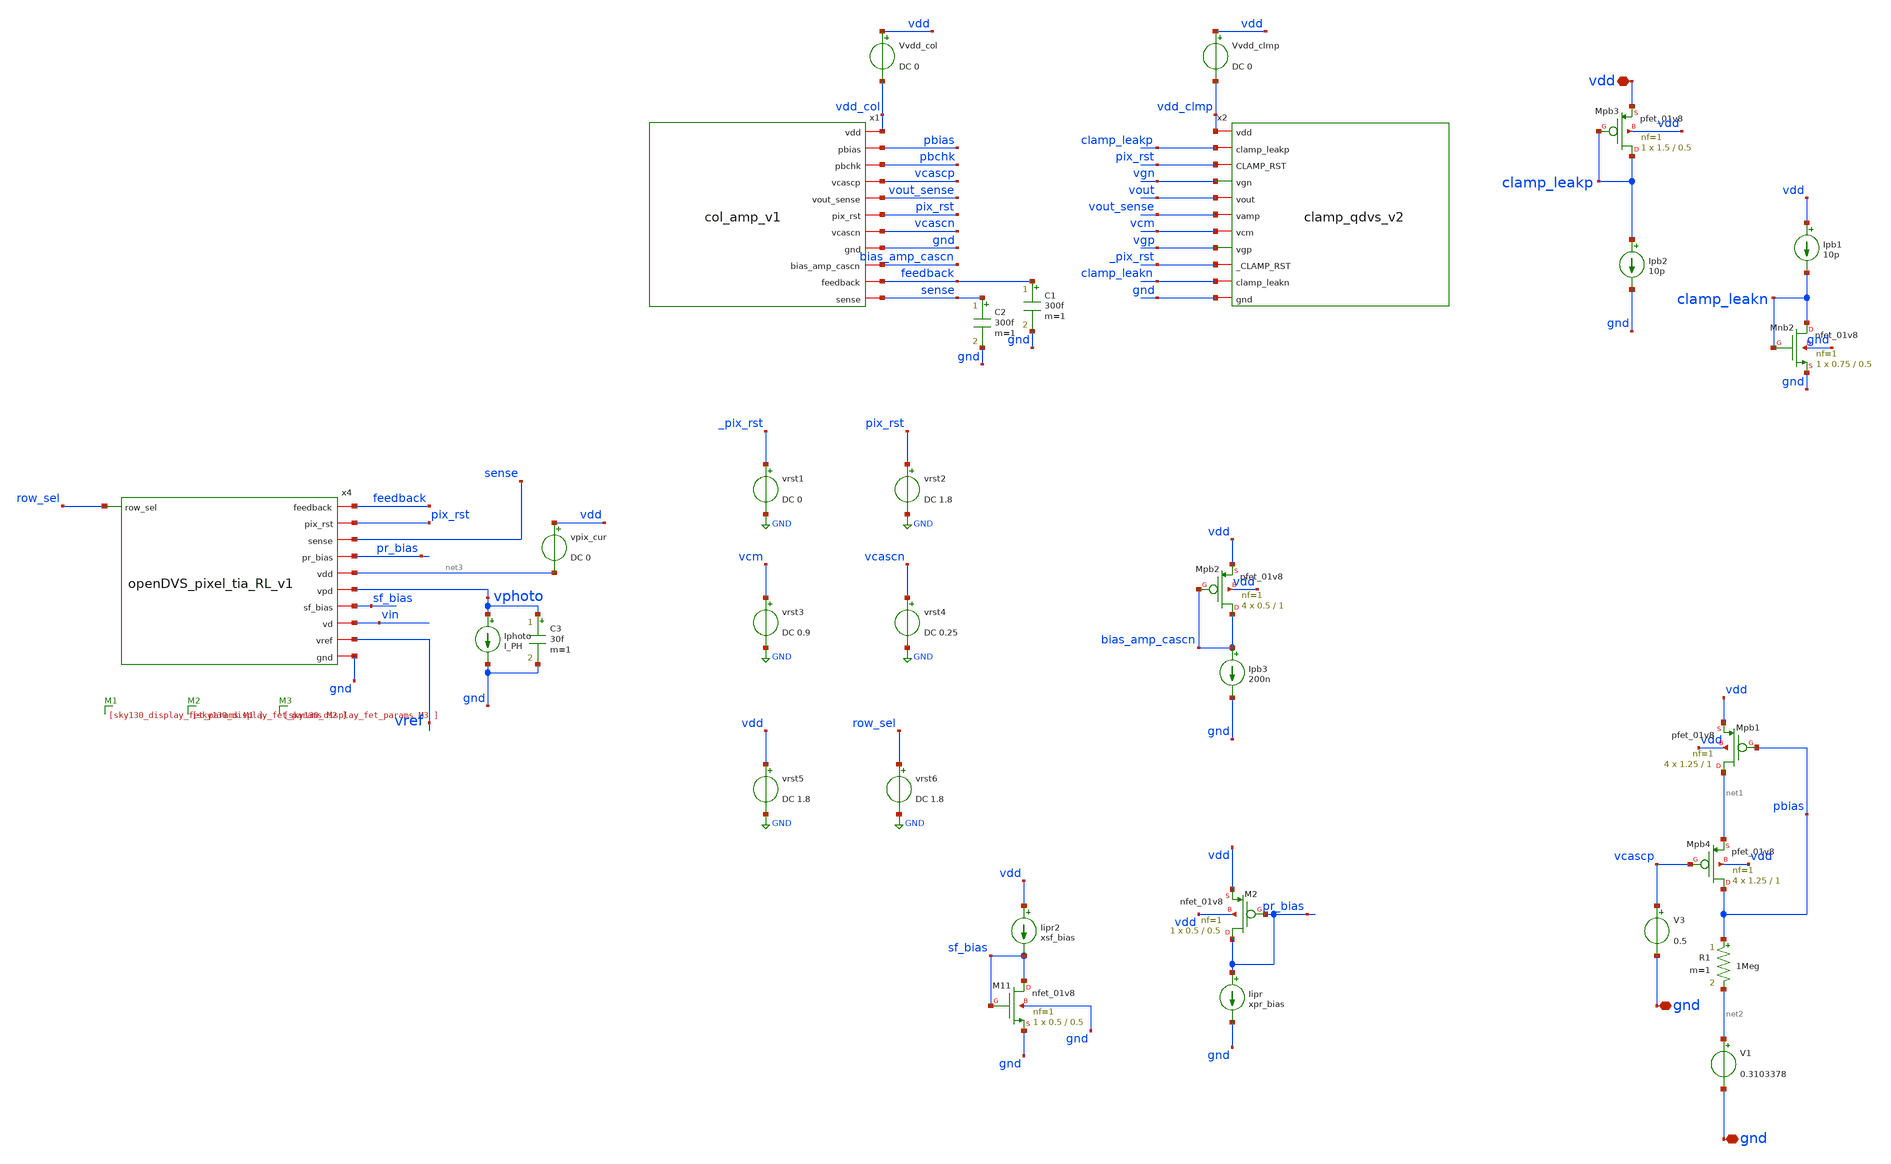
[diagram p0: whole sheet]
** sch_path: analog/xschem/col_amp_n_clamp_v1/Col_Amp_notop_ota_TB.sch
**.subckt Col_Amp_notop_ota_TB vdd gnd gnd
*.iopin vdd
*.iopin gnd
*.iopin gnd
XMpb2 bias_amp_cascn bias_amp_cascn vdd vdd sky130_fd_pr__pfet_01v8 L=1 W=0.5 nf=1 ad='int((1 + 1)/2) * 0.5 / 1 * 0.29'
+ as='int((1 + 2)/2) * 0.5 / 1 * 0.29' pd='2*int((1 + 1)/2) * (0.5 / 1 + 0.29)' ps='2*int((1 + 2)/2) * (0.5 / 1 + 0.29)'
+ nrd='0.29 / 0.5 ' nrs='0.29 / 0.5 ' sa=0 sb=0 sd=0 mult=4 m=4
XMpb3 clamp_leakp clamp_leakp vdd vdd sky130_fd_pr__pfet_01v8 L=0.5 W=1.5 nf=1 ad='int((1 + 1)/2) * 1.5 / 1 * 0.29'
+ as='int((1 + 2)/2) * 1.5 / 1 * 0.29' pd='2*int((1 + 1)/2) * (1.5 / 1 + 0.29)' ps='2*int((1 + 2)/2) * (1.5 / 1 + 0.29)'
+ nrd='0.29 / 1.5 ' nrs='0.29 / 1.5 ' sa=0 sb=0 sd=0 mult=1 m=1
Ipb2 clamp_leakp gnd 10p
vrst3 vcm GND DC 0.9
vrst1 _pix_rst GND DC 0
C1 feedback gnd 300f m=1
C2 sense gnd 300f m=1
Ipb1 vdd clamp_leakn 10p
XMnb2 clamp_leakn clamp_leakn gnd gnd sky130_fd_pr__nfet_01v8 L=0.5 W=0.75 nf=1 ad='int((1 + 1)/2) * 0.75 / 1 * 0.29'
+ as='int((1 + 2)/2) * 0.75 / 1 * 0.29' pd='2*int((1 + 1)/2) * (0.75 / 1 + 0.29)' ps='2*int((1 + 2)/2) * (0.75 / 1 + 0.29)'
+ nrd='0.29 / 0.75 ' nrs='0.29 / 0.75 ' sa=0 sb=0 sd=0 mult=1 m=1
XMpb1 net1 pbias vdd vdd sky130_fd_pr__pfet_01v8 L=1 W=1.25 nf=1 ad='int((1 + 1)/2) * 1.25 / 1 * 0.29'
+ as='int((1 + 2)/2) * 1.25 / 1 * 0.29' pd='2*int((1 + 1)/2) * (1.25 / 1 + 0.29)' ps='2*int((1 + 2)/2) * (1.25 / 1 + 0.29)'
+ nrd='0.29 / 1.25 ' nrs='0.29 / 1.25 ' sa=0 sb=0 sd=0 mult=4 m=4
R1 pbias net2 1Meg m=1
V1 net2 gnd 0.3103378
.save i(v1)
XMpb4 pbias vcascp net1 vdd sky130_fd_pr__pfet_01v8 L=1 W=1.25 nf=1 ad='int((1 + 1)/2) * 1.25 / 1 * 0.29'
+ as='int((1 + 2)/2) * 1.25 / 1 * 0.29' pd='2*int((1 + 1)/2) * (1.25 / 1 + 0.29)' ps='2*int((1 + 2)/2) * (1.25 / 1 + 0.29)'
+ nrd='0.29 / 1.25 ' nrs='0.29 / 1.25 ' sa=0 sb=0 sd=0 mult=4 m=4
V3 vcascp gnd 0.5
.save i(v3)
x1 vdd_col pbias pbchk vcascp vout_sense pix_rst vcascn gnd bias_amp_cascn feedback sense col_amp_v1
x2 vdd_clmp clamp_leakp pix_rst vgn vout vout_sense vcm vgp _pix_rst clamp_leakn gnd clamp_qdvs_v2
C3 vphoto gnd 30f m=1
Iphoto vphoto gnd I_PH
vpix_cur vdd net3 DC 0
.save i(vpix_cur)
x4 feedback pix_rst sense row_sel pr_bias net3 vphoto sf_bias vin vref gnd openDVS_pixel_tia_RL_v1
XM11 sf_bias sf_bias gnd gnd sky130_fd_pr__nfet_01v8 L=0.5 W=0.5 nf=1 ad='int((1 + 1)/2) * 0.5 / 1 * 0.29'
+ as='int((1 + 2)/2) * 0.5 / 1 * 0.29' pd='2*int((1 + 1)/2) * (0.5 / 1 + 0.29)' ps='2*int((1 + 2)/2) * (0.5 / 1 + 0.29)'
+ nrd='0.29 / 0.5 ' nrs='0.29 / 0.5 ' sa=0 sb=0 sd=0 mult=1 m=1
XM2 pr_bias pr_bias vdd vdd sky130_fd_pr__nfet_01v8 L=0.5 W=0.5 nf=1 ad='int((1 + 1)/2) * 0.5 / 1 * 0.29'
+ as='int((1 + 2)/2) * 0.5 / 1 * 0.29' pd='2*int((1 + 1)/2) * (0.5 / 1 + 0.29)' ps='2*int((1 + 2)/2) * (0.5 / 1 + 0.29)'
+ nrd='0.29 / 0.5 ' nrs='0.29 / 0.5 ' sa=0 sb=0 sd=0 mult=1 m=1
Iipr pr_bias gnd xpr_bias
Iipr2 vdd sf_bias xsf_bias
vrst2 pix_rst GND DC 1.8
Ipb3 bias_amp_cascn gnd 200n
vrst4 vcascn GND DC 0.25
vrst5 vdd GND DC 1.8
Vvdd_col vdd vdd_col DC 0
.save i(vvdd_col)
Vvdd_clmp vdd vdd_clmp DC 0
.save i(vvdd_clmp)
vrst6 row_sel GND DC 1.8
**** begin user architecture code

** opencircuitdesign pdks install
.lib $::SKYWATER_MODELS/sky130.lib.spice tt




*INPUT
Vvref vref gnd 0.6 AC 1 0
*Vvref vref gnd 0.6
*Vvin vin gnd DC 0.5903886 AC 1 0

*DC and AC
*Vvin_src vin gnd DC vin_dc AC 0.0001 0
*Settling Time
*Vvin_src vin gnd DC vin_dc PWL(0 0.582 1e-6 0.582 1.01e-6 0.583 15.01e-6 0.583 15.02e-6 0.582
*+ 16.02e-6 0.582)
*Hysteresis
*Vvin_src vin gnd DC vin_dc PWL(0 0 1e-4 0 2e-4 1.8 3e-4 1.8 4e-4 0 5e-4 0)

*SIM
*SET MATRIX SOLVER VARS
.option noopiter=1
.option gmin=1e-15 abstol=1e-15 vntol=1e-9 reltol=1e-6
.option trtol=6 chgtol=1e-16
.option tnom=30 temp=30
.option rshunt = 1.0e12

.save i(Vcol)
.save i(Vclmp)

*.param vin_dc = 0.5825

.param I_PH = 1n
.param xpr_bias=10n
.param xsf_bias=5n
.param xamp_cascn=100n
.param xclmp_lk_p=10p
.param xclmp_lk_n=10p
.param xpix_rst_bias=100n


.control
	save all
	*save v(vout_sense) v(sense) v(pbchk) v(vref) v(vph) v(feedback) v(sense_local)
	*save v(bias_amp_cascn) v(bias_amp_cascp) v(vin)

	*save @m.x1.xmch_amp.msky130_fd_pr__nfet_01v8[gm]

	op
	*print @m.x1.xmnc.msky130_fd_pr__nfet_01v8[vds]
	*print @m.x1.xmch_amp.msky130_fd_pr__nfet_01v8[vds]
	*print @m.x1.xmpc.msky130_fd_pr__pfet_01v8[vds]
	*print @m.x1.xmpb.msky130_fd_pr__pfet_01v8[vds]

	*print @m.x1.xmnc.msky130_fd_pr__nfet_01v8[vdsat]
	*print @m.x1.xmch_amp.msky130_fd_pr__nfet_01v8[vdsat]
	*print @m.x1.xmpc.msky130_fd_pr__pfet_01v8[vdsat]
	*print @m.x1.xmpb.msky130_fd_pr__pfet_01v8[vdsat]

	*print @m.x1.xmnc.msky130_fd_pr__nfet_01v8[vth]
	*print @m.x1.xmch_amp.msky130_fd_pr__nfet_01v8[vth]
	*print @m.x1.xmpc.msky130_fd_pr__pfet_01v8[vth]
	*print @m.x1.xmpb.msky130_fd_pr__pfet_01v8[vth]

	print v(vout_sense)
	print v(vin)
	print i(Vvdd_col)
	print i(Vvdd_clmp)

	*print @m.x1.xmpc.msky130_fd_pr__pfet_01v8[cgg]
	*print @m.x1.xmnc.msky130_fd_pr__nfet_01v8[cgg]


	dc V1 0.0 0.6 0.0001
	plot v(vin) v(vout_sense) v(feedback) v(sense) v(pbchk)
	plot v(vout_sense) - v(vin)

	*meas dc vin_vout when v(vin)=v(vout_sense)
	*meas dc vin_vout_09 when v(vout_sense)=0.9 CROSS=1
	*print vin_vout
	*print vin_vout_09

	*tran 0.1n 25e-6

	*meas tran vin_vout_tup when v(vin)=v(vout_sense) CROSS=1
	*meas tran vin_th_up when v(vout_sense)=1.55 CROSS=1
	*meas tran vin_tmid_up when v(vout_sense)=0.9 CROSS=1
	*meas tran vin_tl_up when v(vout_sense)=0.25 CROSS=1

	*meas tran vin_vout_tdwn when v(vin)=v(vout_sense) CROSS=2
	*meas tran vin_tl_dwn when v(vout_sense)=0.25 CROSS=2
	*meas tran vin_tmid_dwn when v(vout_sense)=0.9 CROSS=2
	*meas tran vin_th_dwn when v(vout_sense)=1.55 CROSS=2


	*meas tran vin_vout_up find v(vin) when v(vout_sense)=v(vin)
	*meas tran vin_h_up find v(vin) when v(vout_sense)=1.55
	*meas tran vin_mid_up find v(vin) when v(vout_sense)=0.9
	*meas tran vin_l_up find v(vin) when v(vout_sense)=0.25

	*meas tran vin_vout_dwn find v(vin) when v(vout_sense)=v(vin)
	*meas tran vin_l_dwn find v(vin) when v(vout_sense)=0.25
	*meas tran vin_mid_dwn find v(vin) when v(vout_sense)=0.9
	*meas tran vin_h_dwn find v(vin) when v(vout_sense)=1.55

	plot v(vin) v(vout_sense)

	write Col_Amp_notop_ota_TB.raw

	*dc Inbias 1n 500n 1n
	*plot v(vin) v(vout_sense) v(feedback) v(sense) v(pbchk)
	*plot v(vout_sense) - v(vin)

	ac dec 100 1 10G
	plot vp(vout_sense) - vp(vin)  xlog
	plot vdb(vout_sense) - vdb(vin) xlog
	plot vdb(vout_sense) vdb(vin) xlog
	plot vp(vout_sense) vp(vin) xlog


	meas ac vout_dcgain find vdb(vout_sense) AT=10
	meas ac vin_dcgain find vdb(vin) AT=10
	let v_gain_bw = vout_dcgain-vin_dcgain - 3
	let vout_sense_db = vdb(vout_sense)
	let vin_db = vdb(vin)
	let vout_db = vout_sense_db - vin_db
	let vout_sense_p = vp(vout_sense)
	let vin_p = vp(vin)
	let vout_p = vout_sense_p - vin_p
	meas ac v_bw when vout_db=v_gain_bw CROSS=1
	meas ac v_p_ft when vout_db=0 CROSS=1
	meas ac vout_ph find vout_p AT=v_p_ft
	let vout_p_pm = 180 - abs(180*vout_ph/pi)
	print vout_p_pm
.endc


**** end user architecture code
**.ends

* expanding   symbol:
*+  /home/user/projects/nic2025_v2/nic2025_openDVS/analog/xschem/col_amp_n_clamp_v1/col_amp_v1.sym # of pins=11
** sym_path: analog/xschem/col_amp_n_clamp_v1/col_amp_v1.sym
** sch_path: analog/xschem/col_amp_n_clamp_v1/col_amp_v1.sch
.subckt col_amp_v1 vdd pbias pbchk vcascp vout_sense pix_rst vcascn gnd bias_amp_cascn feedback
+ sense
*.iopin vdd
*.iopin gnd
*.iopin sense
*.iopin vout_sense
*.iopin feedback
*.iopin pbchk
*.iopin pix_rst
*.iopin vcascn
*.iopin vcascp
*.iopin pbias
*.iopin bias_amp_cascn
XMpb pbchk pbias vdd vdd sky130_fd_pr__pfet_01v8 L=1 W=1.25 nf=1 ad='int((1 + 1)/2) * 1.25 / 1 * 0.29'
+ as='int((1 + 2)/2) * 1.25 / 1 * 0.29' pd='2*int((1 + 1)/2) * (1.25 / 1 + 0.29)' ps='2*int((1 + 2)/2) * (1.25 / 1 + 0.29)'
+ nrd='0.29 / 1.25 ' nrs='0.29 / 1.25 ' sa=0 sb=0 sd=0 mult=1 m=1
XMnc vout_sense amp_p_vg sense gnd sky130_fd_pr__nfet_01v8 L=1 W=0.75 nf=1 ad='int((1 + 1)/2) * 0.75 / 1 * 0.29'
+ as='int((1 + 2)/2) * 0.75 / 1 * 0.29' pd='2*int((1 + 1)/2) * (0.75 / 1 + 0.29)' ps='2*int((1 + 2)/2) * (0.75 / 1 + 0.29)'
+ nrd='0.29 / 0.75 ' nrs='0.29 / 0.75 ' sa=0 sb=0 sd=0 mult=1 m=1
XMfb vout_sense pix_rst feedback gnd sky130_fd_pr__nfet_01v8 L=0.5 W=0.5 nf=1 ad='int((1 + 1)/2) * 0.5 / 1 * 0.29'
+ as='int((1 + 2)/2) * 0.5 / 1 * 0.29' pd='2*int((1 + 1)/2) * (0.5 / 1 + 0.29)' ps='2*int((1 + 2)/2) * (0.5 / 1 + 0.29)'
+ nrd='0.29 / 0.5 ' nrs='0.29 / 0.5 ' sa=0 sb=0 sd=0 mult=1 m=1
XMpc vout_sense vcascp pbchk vdd sky130_fd_pr__pfet_01v8 L=1 W=1.25 nf=1 ad='int((1 + 1)/2) * 1.25 / 1 * 0.29'
+ as='int((1 + 2)/2) * 1.25 / 1 * 0.29' pd='2*int((1 + 1)/2) * (1.25 / 1 + 0.29)' ps='2*int((1 + 2)/2) * (1.25 / 1 + 0.29)'
+ nrd='0.29 / 1.25 ' nrs='0.29 / 1.25 ' sa=0 sb=0 sd=0 mult=1 m=1
XMpb1 pbchk pbias vdd vdd sky130_fd_pr__pfet_01v8 L=1 W=1.25 nf=1 ad='int((1 + 1)/2) * 1.25 / 1 * 0.29'
+ as='int((1 + 2)/2) * 1.25 / 1 * 0.29' pd='2*int((1 + 1)/2) * (1.25 / 1 + 0.29)' ps='2*int((1 + 2)/2) * (1.25 / 1 + 0.29)'
+ nrd='0.29 / 1.25 ' nrs='0.29 / 1.25 ' sa=0 sb=0 sd=0 mult=1 m=1
XMpc1 vout_sense vcascp pbchk vdd sky130_fd_pr__pfet_01v8 L=1 W=1.25 nf=1 ad='int((1 + 1)/2) * 1.25 / 1 * 0.29'
+ as='int((1 + 2)/2) * 1.25 / 1 * 0.29' pd='2*int((1 + 1)/2) * (1.25 / 1 + 0.29)' ps='2*int((1 + 2)/2) * (1.25 / 1 + 0.29)'
+ nrd='0.29 / 1.25 ' nrs='0.29 / 1.25 ' sa=0 sb=0 sd=0 mult=1 m=1
XMpb2 pbchk pbias vdd vdd sky130_fd_pr__pfet_01v8 L=1 W=1.25 nf=1 ad='int((1 + 1)/2) * 1.25 / 1 * 0.29'
+ as='int((1 + 2)/2) * 1.25 / 1 * 0.29' pd='2*int((1 + 1)/2) * (1.25 / 1 + 0.29)' ps='2*int((1 + 2)/2) * (1.25 / 1 + 0.29)'
+ nrd='0.29 / 1.25 ' nrs='0.29 / 1.25 ' sa=0 sb=0 sd=0 mult=1 m=1
XMpc2 vout_sense vcascp pbchk vdd sky130_fd_pr__pfet_01v8 L=1 W=1.25 nf=1 ad='int((1 + 1)/2) * 1.25 / 1 * 0.29'
+ as='int((1 + 2)/2) * 1.25 / 1 * 0.29' pd='2*int((1 + 1)/2) * (1.25 / 1 + 0.29)' ps='2*int((1 + 2)/2) * (1.25 / 1 + 0.29)'
+ nrd='0.29 / 1.25 ' nrs='0.29 / 1.25 ' sa=0 sb=0 sd=0 mult=1 m=1
XMpb3 pbchk pbias vdd vdd sky130_fd_pr__pfet_01v8 L=1 W=1.25 nf=1 ad='int((1 + 1)/2) * 1.25 / 1 * 0.29'
+ as='int((1 + 2)/2) * 1.25 / 1 * 0.29' pd='2*int((1 + 1)/2) * (1.25 / 1 + 0.29)' ps='2*int((1 + 2)/2) * (1.25 / 1 + 0.29)'
+ nrd='0.29 / 1.25 ' nrs='0.29 / 1.25 ' sa=0 sb=0 sd=0 mult=1 m=1
XMpc3 vout_sense vcascp pbchk vdd sky130_fd_pr__pfet_01v8 L=1 W=1.25 nf=1 ad='int((1 + 1)/2) * 1.25 / 1 * 0.29'
+ as='int((1 + 2)/2) * 1.25 / 1 * 0.29' pd='2*int((1 + 1)/2) * (1.25 / 1 + 0.29)' ps='2*int((1 + 2)/2) * (1.25 / 1 + 0.29)'
+ nrd='0.29 / 1.25 ' nrs='0.29 / 1.25 ' sa=0 sb=0 sd=0 mult=1 m=1
XMnc1 vout_sense amp_p_vg sense gnd sky130_fd_pr__nfet_01v8 L=1 W=0.75 nf=1 ad='int((1 + 1)/2) * 0.75 / 1 * 0.29'
+ as='int((1 + 2)/2) * 0.75 / 1 * 0.29' pd='2*int((1 + 1)/2) * (0.75 / 1 + 0.29)' ps='2*int((1 + 2)/2) * (0.75 / 1 + 0.29)'
+ nrd='0.29 / 0.75 ' nrs='0.29 / 0.75 ' sa=0 sb=0 sd=0 mult=1 m=1
XMnc2 vout_sense amp_p_vg sense gnd sky130_fd_pr__nfet_01v8 L=1 W=0.75 nf=1 ad='int((1 + 1)/2) * 0.75 / 1 * 0.29'
+ as='int((1 + 2)/2) * 0.75 / 1 * 0.29' pd='2*int((1 + 1)/2) * (0.75 / 1 + 0.29)' ps='2*int((1 + 2)/2) * (0.75 / 1 + 0.29)'
+ nrd='0.29 / 0.75 ' nrs='0.29 / 0.75 ' sa=0 sb=0 sd=0 mult=1 m=1
XMnc3 vout_sense amp_p_vg sense gnd sky130_fd_pr__nfet_01v8 L=1 W=0.75 nf=1 ad='int((1 + 1)/2) * 0.75 / 1 * 0.29'
+ as='int((1 + 2)/2) * 0.75 / 1 * 0.29' pd='2*int((1 + 1)/2) * (0.75 / 1 + 0.29)' ps='2*int((1 + 2)/2) * (0.75 / 1 + 0.29)'
+ nrd='0.29 / 0.75 ' nrs='0.29 / 0.75 ' sa=0 sb=0 sd=0 mult=1 m=1
xamp vdd amp_p_vg vcascn sense bias_amp_cascn gnd amp_p_5T
.ends


* expanding   symbol:
*+  /home/user/projects/nic2025_v2/nic2025_openDVS/analog/xschem/col_amp_n_clamp_v1/clamp_qdvs_v2.sym # of pins=11
** sym_path: analog/xschem/final/col_amp_n_clamp_v1/clamp_qdvs_v2.sym
** sch_path: analog/xschem/final/col_amp_n_clamp_v1/clamp_qdvs_v2.sch
.subckt clamp_qdvs_v2 vdd clamp_leakp CLAMP_RST vgn vout vamp vcm vgp _CLAMP_RST clamp_leakn gnd
*.iopin vdd
*.iopin gnd
*.iopin vcm
*.iopin _CLAMP_RST
*.iopin CLAMP_RST
*.iopin clamp_leakp
*.iopin clamp_leakn
*.iopin vout
*.iopin vamp
*.opin vgn
*.opin vgp
XM1 vgn vgn vcm gnd sky130_fd_pr__nfet_01v8 L=0.5 W=0.75 nf=1 ad='int((1 + 1)/2) * 0.75 / 1 * 0.29' as='int((1 + 2)/2) * 0.75 / 1 * 0.29'
+ pd='2*int((1 + 1)/2) * (0.75 / 1 + 0.29)' ps='2*int((1 + 2)/2) * (0.75 / 1 + 0.29)' nrd='0.29 / 0.75 '
+ nrs='0.29 / 0.75 ' sa=0 sb=0 sd=0 mult=1 m=1
XM2 vgp vgp vcm vdd sky130_fd_pr__pfet_01v8 L=0.5 W=1.5 nf=1 ad='int((1 + 1)/2) * 1.5 / 1 * 0.29' as='int((1 + 2)/2) * 1.5 / 1 * 0.29'
+ pd='2*int((1 + 1)/2) * (1.5 / 1 + 0.29)' ps='2*int((1 + 2)/2) * (1.5 / 1 + 0.29)' nrd='0.29 / 1.5 ' nrs='0.29 / 1.5 '
+ sa=0 sb=0 sd=0 mult=1 m=1
XM3 vgn clamp_leakp vdd vdd sky130_fd_pr__pfet_01v8 L=0.5 W=1.5 nf=1 ad='int((1 + 1)/2) * 1.5 / 1 * 0.29'
+ as='int((1 + 2)/2) * 1.5 / 1 * 0.29' pd='2*int((1 + 1)/2) * (1.5 / 1 + 0.29)' ps='2*int((1 + 2)/2) * (1.5 / 1 + 0.29)'
+ nrd='0.29 / 1.5 ' nrs='0.29 / 1.5 ' sa=0 sb=0 sd=0 mult=1 m=1
XM4 vgp clamp_leakn gnd gnd sky130_fd_pr__nfet_01v8 L=0.5 W=0.75 nf=1 ad='int((1 + 1)/2) * 0.75 / 1 * 0.29'
+ as='int((1 + 2)/2) * 0.75 / 1 * 0.29' pd='2*int((1 + 1)/2) * (0.75 / 1 + 0.29)' ps='2*int((1 + 2)/2) * (0.75 / 1 + 0.29)'
+ nrd='0.29 / 0.75 ' nrs='0.29 / 0.75 ' sa=0 sb=0 sd=0 mult=1 m=1
XM5 vdd vgn vout gnd sky130_fd_pr__nfet_01v8 L=0.5 W=0.75 nf=1 ad='int((1 + 1)/2) * 0.75 / 1 * 0.29'
+ as='int((1 + 2)/2) * 0.75 / 1 * 0.29' pd='2*int((1 + 1)/2) * (0.75 / 1 + 0.29)' ps='2*int((1 + 2)/2) * (0.75 / 1 + 0.29)'
+ nrd='0.29 / 0.75 ' nrs='0.29 / 0.75 ' sa=0 sb=0 sd=0 mult=1 m=1
XM6 gnd vgp vout vdd sky130_fd_pr__pfet_01v8 L=0.5 W=1.5 nf=1 ad='int((1 + 1)/2) * 1.5 / 1 * 0.29' as='int((1 + 2)/2) * 1.5 / 1 * 0.29'
+ pd='2*int((1 + 1)/2) * (1.5 / 1 + 0.29)' ps='2*int((1 + 2)/2) * (1.5 / 1 + 0.29)' nrd='0.29 / 1.5 ' nrs='0.29 / 1.5 '
+ sa=0 sb=0 sd=0 mult=1 m=1
XM7 vout _CLAMP_RST vamp gnd sky130_fd_pr__nfet_01v8 L=0.5 W=0.75 nf=1 ad='int((1 + 1)/2) * 0.75 / 1 * 0.29'
+ as='int((1 + 2)/2) * 0.75 / 1 * 0.29' pd='2*int((1 + 1)/2) * (0.75 / 1 + 0.29)' ps='2*int((1 + 2)/2) * (0.75 / 1 + 0.29)'
+ nrd='0.29 / 0.75 ' nrs='0.29 / 0.75 ' sa=0 sb=0 sd=0 mult=1 m=1
XM8 vout CLAMP_RST vamp vdd sky130_fd_pr__pfet_01v8 L=0.5 W=1.5 nf=1 ad='int((1 + 1)/2) * 1.5 / 1 * 0.29'
+ as='int((1 + 2)/2) * 1.5 / 1 * 0.29' pd='2*int((1 + 1)/2) * (1.5 / 1 + 0.29)' ps='2*int((1 + 2)/2) * (1.5 / 1 + 0.29)'
+ nrd='0.29 / 1.5 ' nrs='0.29 / 1.5 ' sa=0 sb=0 sd=0 mult=1 m=1
.ends


* expanding   symbol:
*+  /home/user/projects/nic2025_v2/nic2025_openDVS/analog/xschem/col_amp_n_clamp_v1/openDVS_pixel_tia_RL_v1.sym # of pins=11
** sym_path: analog/xschem/col_amp_n_clamp_v1/openDVS_pixel_tia_RL_v1.sym
** sch_path: analog/xschem/col_amp_n_clamp_v1/openDVS_pixel_tia_RL_v1.sch
.subckt openDVS_pixel_tia_RL_v1 feedback pix_rst sense row_sel pr_bias vdd vpd sf_bias vd vref gnd
*.ipin row_sel
*.iopin sense
*.iopin pix_rst
*.iopin feedback
*.iopin pr_bias
*.iopin vdd
*.iopin vref
*.iopin vpd
*.iopin sf_bias
*.iopin gnd
*.iopin vd
XCSAMPLE vph_sf vd sky130_fd_pr__cap_mim_m3_1 W=1 L=1 MF=8 m=8
XCREF vref vd sky130_fd_pr__cap_mim_m3_1 W=1 L=1 MF=2 m=2
XMpd vdd vpr vpd gnd sky130_fd_pr__nfet_01v8 L=0.5 W=0.5 nf=1 ad='int((1 + 1)/2) * 0.5 / 1 * 0.29' as='int((1 + 2)/2) * 0.5 / 1 * 0.29'
+ pd='2*int((1 + 1)/2) * (0.5 / 1 + 0.29)' ps='2*int((1 + 2)/2) * (0.5 / 1 + 0.29)' nrd='0.29 / 0.5 ' nrs='0.29 / 0.5 '
+ sa=0 sb=0 sd=0 mult=1 m=1
XMch_amp sense_local vd gnd gnd sky130_fd_pr__nfet_01v8 L=1 W=2 nf=1 ad='int((1 + 1)/2) * 2 / 1 * 0.29'
+ as='int((1 + 2)/2) * 2 / 1 * 0.29' pd='2*int((1 + 1)/2) * (2 / 1 + 0.29)' ps='2*int((1 + 2)/2) * (2 / 1 + 0.29)'
+ nrd='0.29 / 2 ' nrs='0.29 / 2 ' sa=0 sb=0 sd=0 mult=1 m=1
XMsw gnd gnd gnd gnd sky130_fd_pr__nfet_01v8 L=0.75 W=0.75 nf=1 ad='int((1 + 1)/2) * 0.75 / 1 * 0.29'
+ as='int((1 + 2)/2) * 0.75 / 1 * 0.29' pd='2*int((1 + 1)/2) * (0.75 / 1 + 0.29)' ps='2*int((1 + 2)/2) * (0.75 / 1 + 0.29)'
+ nrd='0.29 / 0.75 ' nrs='0.29 / 0.75 ' sa=0 sb=0 sd=0 mult=1 m=1
XMsf_bias vph_sf sf_bias gnd gnd sky130_fd_pr__nfet_01v8 L=0.5 W=0.5 nf=1 ad='int((1 + 1)/2) * 0.5 / 1 * 0.29'
+ as='int((1 + 2)/2) * 0.5 / 1 * 0.29' pd='2*int((1 + 1)/2) * (0.5 / 1 + 0.29)' ps='2*int((1 + 2)/2) * (0.5 / 1 + 0.29)'
+ nrd='0.29 / 0.5 ' nrs='0.29 / 0.5 ' sa=0 sb=0 sd=0 mult=1 m=1
XMsf vdd vpr vph_sf gnd sky130_fd_pr__nfet_01v8 L=0.5 W=0.5 nf=1 ad='int((1 + 1)/2) * 0.5 / 1 * 0.29'
+ as='int((1 + 2)/2) * 0.5 / 1 * 0.29' pd='2*int((1 + 1)/2) * (0.5 / 1 + 0.29)' ps='2*int((1 + 2)/2) * (0.5 / 1 + 0.29)'
+ nrd='0.29 / 0.5 ' nrs='0.29 / 0.5 ' sa=0 sb=0 sd=0 mult=1 m=1
XMrow_sel sense row_sel sense_local gnd sky130_fd_pr__nfet_01v8 L=0.2 W=0.5 nf=1 ad='int((1 + 1)/2) * 0.5 / 1 * 0.29'
+ as='int((1 + 2)/2) * 0.5 / 1 * 0.29' pd='2*int((1 + 1)/2) * (0.5 / 1 + 0.29)' ps='2*int((1 + 2)/2) * (0.5 / 1 + 0.29)'
+ nrd='0.29 / 0.5 ' nrs='0.29 / 0.5 ' sa=0 sb=0 sd=0 mult=1 m=1
XMfb_row_sel pix_rst row_sel lrst gnd sky130_fd_pr__nfet_01v8 L=0.5 W=0.5 nf=1 ad='int((1 + 1)/2) * 0.5 / 1 * 0.29'
+ as='int((1 + 2)/2) * 0.5 / 1 * 0.29' pd='2*int((1 + 1)/2) * (0.5 / 1 + 0.29)' ps='2*int((1 + 2)/2) * (0.5 / 1 + 0.29)'
+ nrd='0.29 / 0.5 ' nrs='0.29 / 0.5 ' sa=0 sb=0 sd=0 mult=1 m=1
XMpr_amp vpr vpd gnd gnd sky130_fd_pr__nfet_01v8 L=0.5 W=0.5 nf=1 ad='int((1 + 1)/2) * 0.5 / 1 * 0.29'
+ as='int((1 + 2)/2) * 0.5 / 1 * 0.29' pd='2*int((1 + 1)/2) * (0.5 / 1 + 0.29)' ps='2*int((1 + 2)/2) * (0.5 / 1 + 0.29)'
+ nrd='0.29 / 0.5 ' nrs='0.29 / 0.5 ' sa=0 sb=0 sd=0 mult=1 m=1
XMpr_bias vpr pr_bias vdd vdd sky130_fd_pr__nfet_01v8 L=0.5 W=0.5 nf=1 ad='int((1 + 1)/2) * 0.5 / 1 * 0.29'
+ as='int((1 + 2)/2) * 0.5 / 1 * 0.29' pd='2*int((1 + 1)/2) * (0.5 / 1 + 0.29)' ps='2*int((1 + 2)/2) * (0.5 / 1 + 0.29)'
+ nrd='0.29 / 0.5 ' nrs='0.29 / 0.5 ' sa=0 sb=0 sd=0 mult=1 m=1
XD1 gnd vpd sky130_fd_pr__photodiode area=25 perim=20
S2 gnd gnd gnd gnd SW1
XMsw1 feedback lrst vd gnd sky130_fd_pr__nfet_01v8 L=0.75 W=0.75 nf=1 ad='int((1 + 1)/2) * 0.75 / 1 * 0.29'
+ as='int((1 + 2)/2) * 0.75 / 1 * 0.29' pd='2*int((1 + 1)/2) * (0.75 / 1 + 0.29)' ps='2*int((1 + 2)/2) * (0.75 / 1 + 0.29)'
+ nrd='0.29 / 0.75 ' nrs='0.29 / 0.75 ' sa=0 sb=0 sd=0 mult=1 m=1
.ends


* expanding   symbol:  col_amp_n_clamp_v1/amp_p_5T.sym # of pins=6
** sym_path: analog/xschem/final/col_amp_n_clamp_v1/amp_p_5T.sym
** sch_path: analog/xschem/final/col_amp_n_clamp_v1/amp_p_5T.sch
.subckt amp_p_5T vdd vout vp vm vbias gnd
*.iopin gnd
*.iopin vdd
*.iopin vout
*.iopin vm
*.iopin vp
*.iopin vbias
XMinm vout vm vsource vdd sky130_fd_pr__pfet_01v8 L=0.2 W=0.5 nf=1 ad='int((1 + 1)/2) * 0.5 / 1 * 0.29'
+ as='int((1 + 2)/2) * 0.5 / 1 * 0.29' pd='2*int((1 + 1)/2) * (0.5 / 1 + 0.29)' ps='2*int((1 + 2)/2) * (0.5 / 1 + 0.29)'
+ nrd='0.29 / 0.5 ' nrs='0.29 / 0.5 ' sa=0 sb=0 sd=0 mult=1 m=1
XMinp vdio vp vsource vdd sky130_fd_pr__pfet_01v8 L=0.2 W=0.5 nf=1 ad='int((1 + 1)/2) * 0.5 / 1 * 0.29'
+ as='int((1 + 2)/2) * 0.5 / 1 * 0.29' pd='2*int((1 + 1)/2) * (0.5 / 1 + 0.29)' ps='2*int((1 + 2)/2) * (0.5 / 1 + 0.29)'
+ nrd='0.29 / 0.5 ' nrs='0.29 / 0.5 ' sa=0 sb=0 sd=0 mult=1 m=1
XMdio vdio vdio gnd gnd sky130_fd_pr__nfet_01v8 L=0.2 W=0.5 nf=1 ad='int((1 + 1)/2) * 0.5 / 1 * 0.29'
+ as='int((1 + 2)/2) * 0.5 / 1 * 0.29' pd='2*int((1 + 1)/2) * (0.5 / 1 + 0.29)' ps='2*int((1 + 2)/2) * (0.5 / 1 + 0.29)'
+ nrd='0.29 / 0.5 ' nrs='0.29 / 0.5 ' sa=0 sb=0 sd=0 mult=1 m=1
XMmirr vout vdio gnd gnd sky130_fd_pr__nfet_01v8 L=0.2 W=0.5 nf=1 ad='int((1 + 1)/2) * 0.5 / 1 * 0.29'
+ as='int((1 + 2)/2) * 0.5 / 1 * 0.29' pd='2*int((1 + 1)/2) * (0.5 / 1 + 0.29)' ps='2*int((1 + 2)/2) * (0.5 / 1 + 0.29)'
+ nrd='0.29 / 0.5 ' nrs='0.29 / 0.5 ' sa=0 sb=0 sd=0 mult=1 m=1
XMbias vsource vbias vdd vdd sky130_fd_pr__pfet_01v8 L=1 W=1 nf=1 ad='int((1 + 1)/2) * 1 / 1 * 0.29'
+ as='int((1 + 2)/2) * 1 / 1 * 0.29' pd='2*int((1 + 1)/2) * (1 / 1 + 0.29)' ps='2*int((1 + 2)/2) * (1 / 1 + 0.29)'
+ nrd='0.29 / 1 ' nrs='0.29 / 1 ' sa=0 sb=0 sd=0 mult=1 m=1
.ends

.GLOBAL GND
**** begin user architecture code
.MODEL SW1 SW   VT=0.9 VH=0.01  RON=0.01 ROFF=10G
**** end user architecture code
.end
